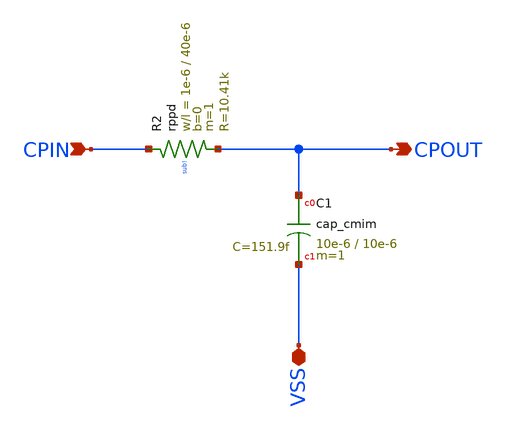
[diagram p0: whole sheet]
** sch_path: Cells/CP.sch
**.subckt CP VSS CPIN CPOUT
*.iopin VSS
*.ipin CPIN
*.opin CPOUT
XC1 CPOUT VSS cap_cmim w=10e-6 l=10e-6 m=1 mm_ok=1
XR2 CPIN CPOUT sub! rppd w=1e-6 l=40e-6 m=1 b=0 mm_ok=1
**.ends
.end
